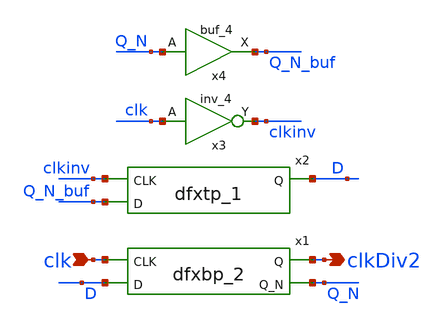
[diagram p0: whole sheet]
** sch_path: xschem/lib/DLib_freqDiv2.sch
**.subckt DLib_freqDiv2 clkDiv2 clk
*.opin clkDiv2
*.ipin clk
x1 clk D VGND VNB VPB VPWR clkDiv2 Q_N sky130_fd_sc_hd__dfxbp_2
x2 clkinv Q_N_buf VGND VGND VPWR VPWR D sky130_fd_sc_hd__dfxtp_1
x3 clk VGND VGND VPWR VPWR clkinv sky130_fd_sc_hd__inv_4
x4 Q_N VGND VGND VPWR VPWR Q_N_buf sky130_fd_sc_hd__buf_4
**.ends
.end
